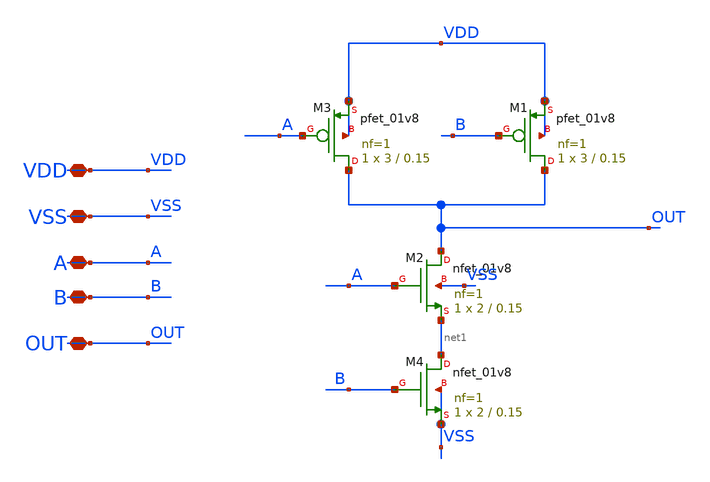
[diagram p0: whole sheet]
** sch_path: xschem/DC_DC_Converter_xschem/OTHERS/DC_DC_Converter_JV8/NAND_GATE/NAND.sch
**.subckt NAND VDD VSS A B OUT
*.iopin VDD
*.iopin VSS
*.iopin A
*.iopin B
*.iopin OUT
XM2 OUT A net1 VSS sky130_fd_pr__nfet_01v8 L=0.15 W=2 nf=1 ad='int((nf+1)/2) * W/nf * 0.29' as='int((nf+2)/2) * W/nf * 0.29'
+ pd='2*int((nf+1)/2) * (W/nf + 0.29)' ps='2*int((nf+2)/2) * (W/nf + 0.29)' nrd='0.29 / W' nrs='0.29 / W'
+ sa=0 sb=0 sd=0 mult=1 m=1
XM3 OUT A VDD VDD sky130_fd_pr__pfet_01v8 L=0.15 W=3 nf=1 ad='int((nf+1)/2) * W/nf * 0.29' as='int((nf+2)/2) * W/nf * 0.29'
+ pd='2*int((nf+1)/2) * (W/nf + 0.29)' ps='2*int((nf+2)/2) * (W/nf + 0.29)' nrd='0.29 / W' nrs='0.29 / W'
+ sa=0 sb=0 sd=0 mult=1 m=1
XM1 OUT B VDD VDD sky130_fd_pr__pfet_01v8 L=0.15 W=3 nf=1 ad='int((nf+1)/2) * W/nf * 0.29' as='int((nf+2)/2) * W/nf * 0.29'
+ pd='2*int((nf+1)/2) * (W/nf + 0.29)' ps='2*int((nf+2)/2) * (W/nf + 0.29)' nrd='0.29 / W' nrs='0.29 / W'
+ sa=0 sb=0 sd=0 mult=1 m=1
XM4 net1 B VSS VSS sky130_fd_pr__nfet_01v8 L=0.15 W=2 nf=1 ad='int((nf+1)/2) * W/nf * 0.29' as='int((nf+2)/2) * W/nf * 0.29'
+ pd='2*int((nf+1)/2) * (W/nf + 0.29)' ps='2*int((nf+2)/2) * (W/nf + 0.29)' nrd='0.29 / W' nrs='0.29 / W'
+ sa=0 sb=0 sd=0 mult=1 m=1
**.ends
.end
